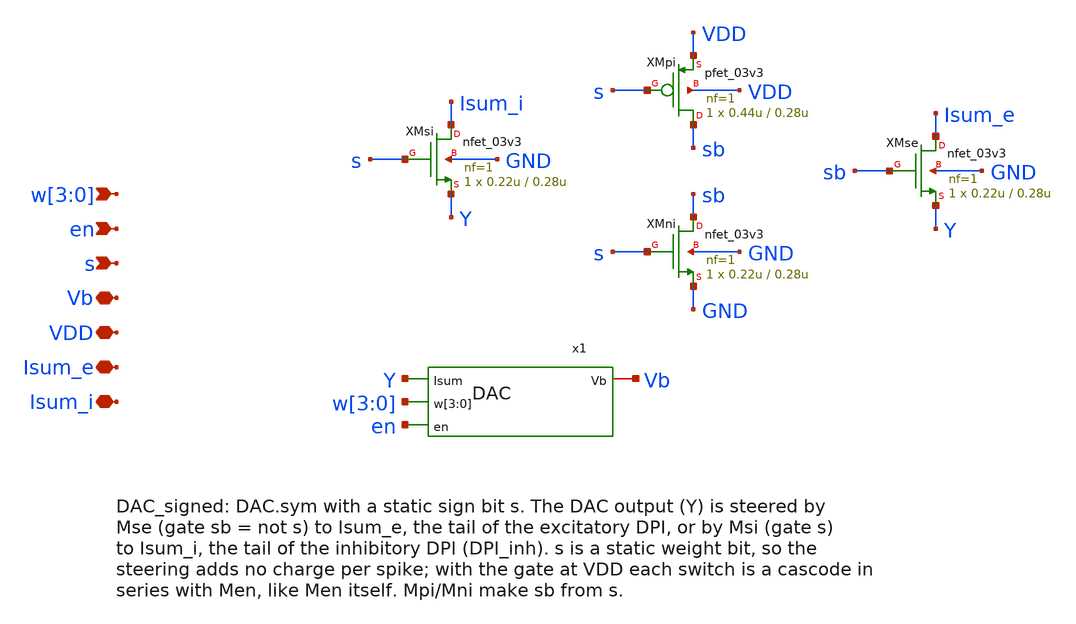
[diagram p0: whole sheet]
** sch_path: analog/neuron/DAC_signed.sch
**.subckt DAC_signed w[3],w[2],w[1],w[0] en s Vb VDD Isum_e Isum_i
*.ipin w[3],w[2],w[1],w[0]
*.ipin en
*.ipin s
*.iopin Vb
*.iopin VDD
*.iopin Isum_e
*.iopin Isum_i
x1 Y Vb w[3] w[2] w[1] w[0] en DAC
XMse Isum_e sb Y GND nfet_03v3 L=0.28u W=0.22u nf=1 ad='int((nf+1)/2) * W/nf * 0.18u' as='int((nf+2)/2) * W/nf * 0.18u'
+ pd='2*int((nf+1)/2) * (W/nf + 0.18u)' ps='2*int((nf+2)/2) * (W/nf + 0.18u)' nrd='0.18u / W' nrs='0.18u / W'
+ sa=0 sb=0 sd=0 m=1
XMsi Isum_i s Y GND nfet_03v3 L=0.28u W=0.22u nf=1 ad='int((nf+1)/2) * W/nf * 0.18u' as='int((nf+2)/2) * W/nf * 0.18u'
+ pd='2*int((nf+1)/2) * (W/nf + 0.18u)' ps='2*int((nf+2)/2) * (W/nf + 0.18u)' nrd='0.18u / W' nrs='0.18u / W'
+ sa=0 sb=0 sd=0 m=1
XMpi sb s VDD VDD pfet_03v3 L=0.28u W=0.44u nf=1 ad='int((nf+1)/2) * W/nf * 0.18u' as='int((nf+2)/2) * W/nf * 0.18u'
+ pd='2*int((nf+1)/2) * (W/nf + 0.18u)' ps='2*int((nf+2)/2) * (W/nf + 0.18u)' nrd='0.18u / W' nrs='0.18u / W'
+ sa=0 sb=0 sd=0 m=1
XMni sb s GND GND nfet_03v3 L=0.28u W=0.22u nf=1 ad='int((nf+1)/2) * W/nf * 0.18u' as='int((nf+2)/2) * W/nf * 0.18u'
+ pd='2*int((nf+1)/2) * (W/nf + 0.18u)' ps='2*int((nf+2)/2) * (W/nf + 0.18u)' nrd='0.18u / W' nrs='0.18u / W'
+ sa=0 sb=0 sd=0 m=1
**.ends

* expanding   symbol:  DAC.sym # of pins=4
** sym_path: analog/neuron/DAC.sym
** sch_path: analog/neuron/DAC.sch
.subckt DAC Isum Vb w[3] w[2] w[1] w[0] en
*.iopin Vb
*.ipin w[3],w[2],w[1],w[0]
*.ipin Isum
*.ipin en
XM1 X w[0] net4 net4 nfet_03v3 L=0.28u W=0.22u nf=1 ad='int((nf+1)/2) * W/nf * 0.18u' as='int((nf+2)/2) * W/nf * 0.18u'
+ pd='2*int((nf+1)/2) * (W/nf + 0.18u)' ps='2*int((nf+2)/2) * (W/nf + 0.18u)' nrd='0.18u / W' nrs='0.18u / W'
+ sa=0 sb=0 sd=0 m=1
XM2 net4 Vb GND GND nfet_03v3 L=8u W=1u nf=1 ad='int((nf+1)/2) * W/nf * 0.18u' as='int((nf+2)/2) * W/nf * 0.18u'
+ pd='2*int((nf+1)/2) * (W/nf + 0.18u)' ps='2*int((nf+2)/2) * (W/nf + 0.18u)' nrd='0.18u / W' nrs='0.18u / W'
+ sa=0 sb=0 sd=0 m=1
XM3 X w[1] net2 net2 nfet_03v3 L=0.28u W=0.22u nf=1 ad='int((nf+1)/2) * W/nf * 0.18u' as='int((nf+2)/2) * W/nf * 0.18u'
+ pd='2*int((nf+1)/2) * (W/nf + 0.18u)' ps='2*int((nf+2)/2) * (W/nf + 0.18u)' nrd='0.18u / W' nrs='0.18u / W'
+ sa=0 sb=0 sd=0 m=2
XM4 net2 Vb GND GND nfet_03v3 L=8u W=1u nf=1 ad='int((nf+1)/2) * W/nf * 0.18u' as='int((nf+2)/2) * W/nf * 0.18u'
+ pd='2*int((nf+1)/2) * (W/nf + 0.18u)' ps='2*int((nf+2)/2) * (W/nf + 0.18u)' nrd='0.18u / W' nrs='0.18u / W'
+ sa=0 sb=0 sd=0 m=2
XM5 X w[2] net3 net3 nfet_03v3 L=0.28u W=0.22u nf=1 ad='int((nf+1)/2) * W/nf * 0.18u' as='int((nf+2)/2) * W/nf * 0.18u'
+ pd='2*int((nf+1)/2) * (W/nf + 0.18u)' ps='2*int((nf+2)/2) * (W/nf + 0.18u)' nrd='0.18u / W' nrs='0.18u / W'
+ sa=0 sb=0 sd=0 m=3
XM6 net3 Vb GND GND nfet_03v3 L=8u W=1u nf=1 ad='int((nf+1)/2) * W/nf * 0.18u' as='int((nf+2)/2) * W/nf * 0.18u'
+ pd='2*int((nf+1)/2) * (W/nf + 0.18u)' ps='2*int((nf+2)/2) * (W/nf + 0.18u)' nrd='0.18u / W' nrs='0.18u / W'
+ sa=0 sb=0 sd=0 m=3
XM7 X w[3] net1 net1 nfet_03v3 L=0.28u W=0.22u nf=1 ad='int((nf+1)/2) * W/nf * 0.18u' as='int((nf+2)/2) * W/nf * 0.18u'
+ pd='2*int((nf+1)/2) * (W/nf + 0.18u)' ps='2*int((nf+2)/2) * (W/nf + 0.18u)' nrd='0.18u / W' nrs='0.18u / W'
+ sa=0 sb=0 sd=0 m=4
XM8 net1 Vb GND GND nfet_03v3 L=8u W=1u nf=1 ad='int((nf+1)/2) * W/nf * 0.18u' as='int((nf+2)/2) * W/nf * 0.18u'
+ pd='2*int((nf+1)/2) * (W/nf + 0.18u)' ps='2*int((nf+2)/2) * (W/nf + 0.18u)' nrd='0.18u / W' nrs='0.18u / W'
+ sa=0 sb=0 sd=0 m=4
XMen Isum en X GND nfet_03v3 L=0.28u W=0.22u nf=1 ad='int((nf+1)/2) * W/nf * 0.18u' as='int((nf+2)/2) * W/nf * 0.18u'
+ pd='2*int((nf+1)/2) * (W/nf + 0.18u)' ps='2*int((nf+2)/2) * (W/nf + 0.18u)' nrd='0.18u / W' nrs='0.18u / W'
+ sa=0 sb=0 sd=0 m=1
.ends

.GLOBAL GND
.end
